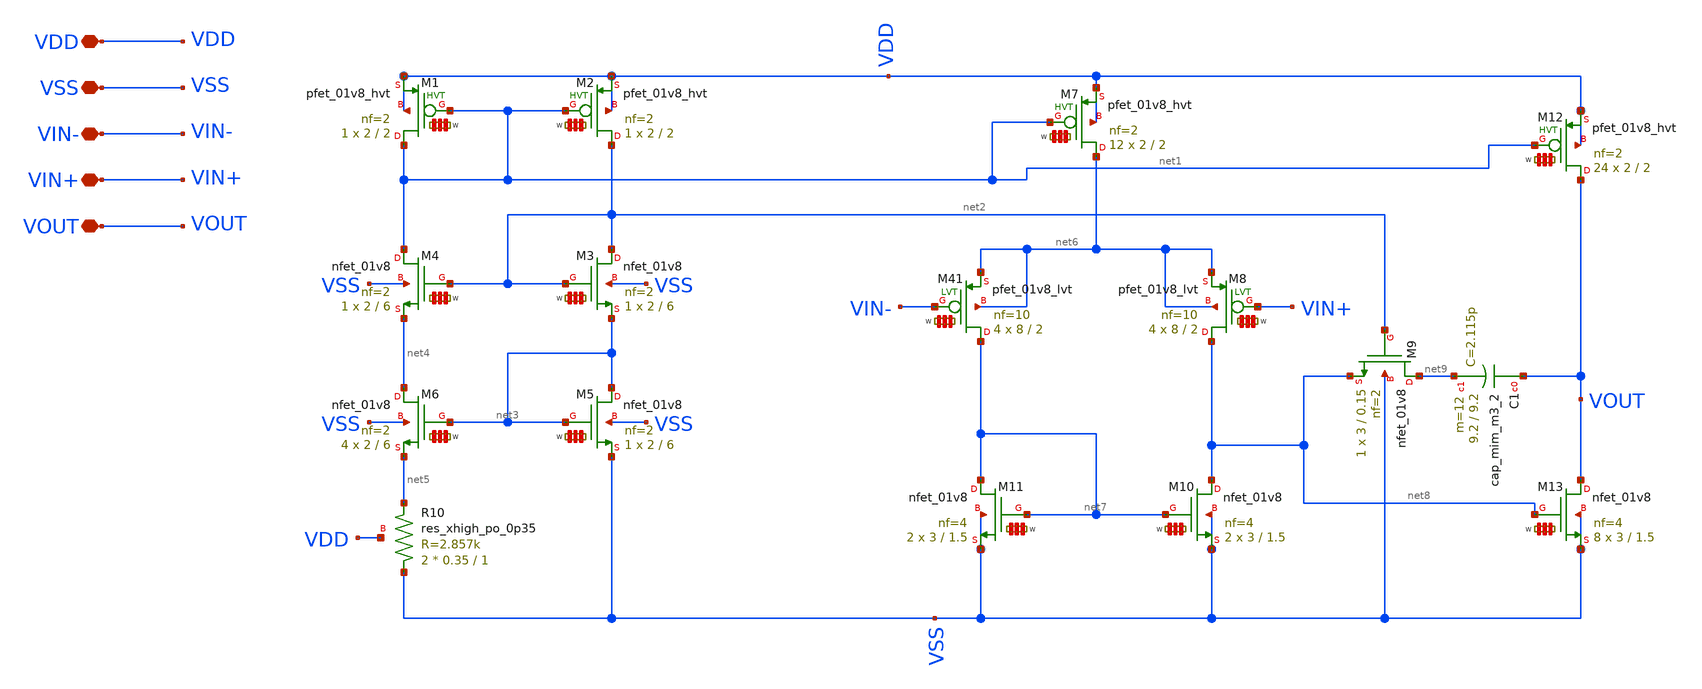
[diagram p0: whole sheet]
** sch_path: my_ip/sky130A/PMOS_2_stage_1_8_opamp_V1/op_amp.sch
**.subckt op_amp VDD VSS VIN- VIN+ VOUT
*.iopin VDD
*.iopin VSS
*.iopin VIN-
*.iopin VIN+
*.iopin VOUT
XM5 net3 net3 VSS VSS sky130_fd_pr__nfet_01v8 L=6 W='2 * 2 ' nf=2 ad='int((2 + 1)/2) * 2 / 2 * 0.29'
+ as='int((2 + 2)/2) * 2 / 2 * 0.29' pd='2*int((2 + 1)/2) * (2 / 2 + 0.29)' ps='2*int((2 + 2)/2) * (2 / 2 + 0.29)'
+ nrd='0.29 / 2 ' nrs='0.29 / 2 ' sa=0 sb=0 sd=0 mult=1 m=1
XM6 net4 net3 net5 VSS sky130_fd_pr__nfet_01v8 L=6 W='2 * 2 ' nf=2 ad='int((2 + 1)/2) * 2 / 2 * 0.29'
+ as='int((2 + 2)/2) * 2 / 2 * 0.29' pd='2*int((2 + 1)/2) * (2 / 2 + 0.29)' ps='2*int((2 + 2)/2) * (2 / 2 + 0.29)'
+ nrd='0.29 / 2 ' nrs='0.29 / 2 ' sa=0 sb=0 sd=0 mult=4 m=4
XM7 net6 net1 VDD VDD sky130_fd_pr__pfet_01v8_hvt L=2 W='2 * 2 ' nf=2 ad='int((2 + 1)/2) * 2 / 2 * 0.29'
+ as='int((2 + 2)/2) * 2 / 2 * 0.29' pd='2*int((2 + 1)/2) * (2 / 2 + 0.29)' ps='2*int((2 + 2)/2) * (2 / 2 + 0.29)'
+ nrd='0.29 / 2 ' nrs='0.29 / 2 ' sa=0 sb=0 sd=0 mult=12 m=12
XM2 net2 net1 VDD VDD sky130_fd_pr__pfet_01v8_hvt L=2 W='2 * 2 ' nf=2 ad='int((2 + 1)/2) * 2 / 2 * 0.29'
+ as='int((2 + 2)/2) * 2 / 2 * 0.29' pd='2*int((2 + 1)/2) * (2 / 2 + 0.29)' ps='2*int((2 + 2)/2) * (2 / 2 + 0.29)'
+ nrd='0.29 / 2 ' nrs='0.29 / 2 ' sa=0 sb=0 sd=0 mult=1 m=1
XM1 net1 net1 VDD VDD sky130_fd_pr__pfet_01v8_hvt L=2 W='2 * 2 ' nf=2 ad='int((2 + 1)/2) * 2 / 2 * 0.29'
+ as='int((2 + 2)/2) * 2 / 2 * 0.29' pd='2*int((2 + 1)/2) * (2 / 2 + 0.29)' ps='2*int((2 + 2)/2) * (2 / 2 + 0.29)'
+ nrd='0.29 / 2 ' nrs='0.29 / 2 ' sa=0 sb=0 sd=0 mult=1 m=1
XR10 VSS net5 VDD sky130_fd_pr__res_xhigh_po_0p35 L=1 mult=2 m=2
XM4 net1 net2 net4 VSS sky130_fd_pr__nfet_01v8 L=6 W='2 * 2 ' nf=2 ad='int((2 + 1)/2) * 2 / 2 * 0.29'
+ as='int((2 + 2)/2) * 2 / 2 * 0.29' pd='2*int((2 + 1)/2) * (2 / 2 + 0.29)' ps='2*int((2 + 2)/2) * (2 / 2 + 0.29)'
+ nrd='0.29 / 2 ' nrs='0.29 / 2 ' sa=0 sb=0 sd=0 mult=1 m=1
XM3 net2 net2 net3 VSS sky130_fd_pr__nfet_01v8 L=6 W='2 * 2 ' nf=2 ad='int((2 + 1)/2) * 2 / 2 * 0.29'
+ as='int((2 + 2)/2) * 2 / 2 * 0.29' pd='2*int((2 + 1)/2) * (2 / 2 + 0.29)' ps='2*int((2 + 2)/2) * (2 / 2 + 0.29)'
+ nrd='0.29 / 2 ' nrs='0.29 / 2 ' sa=0 sb=0 sd=0 mult=1 m=1
XM10 net8 net7 VSS VSS sky130_fd_pr__nfet_01v8 L=1.5 W='3 * 4 ' nf=4 ad='int((4 + 1)/2) * 3 / 4 * 0.29'
+ as='int((4 + 2)/2) * 3 / 4 * 0.29' pd='2*int((4 + 1)/2) * (3 / 4 + 0.29)' ps='2*int((4 + 2)/2) * (3 / 4 + 0.29)'
+ nrd='0.29 / 3 ' nrs='0.29 / 3 ' sa=0 sb=0 sd=0 mult=2 m=2
XM11 net7 net7 VSS VSS sky130_fd_pr__nfet_01v8 L=1.5 W='3 * 4 ' nf=4 ad='int((4 + 1)/2) * 3 / 4 * 0.29'
+ as='int((4 + 2)/2) * 3 / 4 * 0.29' pd='2*int((4 + 1)/2) * (3 / 4 + 0.29)' ps='2*int((4 + 2)/2) * (3 / 4 + 0.29)'
+ nrd='0.29 / 3 ' nrs='0.29 / 3 ' sa=0 sb=0 sd=0 mult=2 m=2
XM12 VOUT net1 VDD VDD sky130_fd_pr__pfet_01v8_hvt L=2 W='2 * 2 ' nf=2 ad='int((2 + 1)/2) * 2 / 2 * 0.29'
+ as='int((2 + 2)/2) * 2 / 2 * 0.29' pd='2*int((2 + 1)/2) * (2 / 2 + 0.29)' ps='2*int((2 + 2)/2) * (2 / 2 + 0.29)'
+ nrd='0.29 / 2 ' nrs='0.29 / 2 ' sa=0 sb=0 sd=0 mult=24 m=24
XM13 VOUT net8 VSS VSS sky130_fd_pr__nfet_01v8 L=1.5 W='3 * 4 ' nf=4 ad='int((4 + 1)/2) * 3 / 4 * 0.29'
+ as='int((4 + 2)/2) * 3 / 4 * 0.29' pd='2*int((4 + 1)/2) * (3 / 4 + 0.29)' ps='2*int((4 + 2)/2) * (3 / 4 + 0.29)'
+ nrd='0.29 / 3 ' nrs='0.29 / 3 ' sa=0 sb=0 sd=0 mult=8 m=8
XC1 VOUT net9 sky130_fd_pr__cap_mim_m3_2 W=9.2 L=9.2 MF=12 m=12
XM41 net7 VIN- net6 net6 sky130_fd_pr__pfet_01v8_lvt L=2 W='8 * 10 ' nf=10 ad='int((10 + 1)/2) * 8 / 10 * 0.29'
+ as='int((10 + 2)/2) * 8 / 10 * 0.29' pd='2*int((10 + 1)/2) * (8 / 10 + 0.29)' ps='2*int((10 + 2)/2) * (8 / 10 + 0.29)'
+ nrd='0.29 / 8 ' nrs='0.29 / 8 ' sa=0 sb=0 sd=0 mult=4 m=4
XM8 net8 VIN+ net6 net6 sky130_fd_pr__pfet_01v8_lvt L=2 W='8 * 10 ' nf=10 ad='int((10 + 1)/2) * 8 / 10 * 0.29'
+ as='int((10 + 2)/2) * 8 / 10 * 0.29' pd='2*int((10 + 1)/2) * (8 / 10 + 0.29)' ps='2*int((10 + 2)/2) * (8 / 10 + 0.29)'
+ nrd='0.29 / 8 ' nrs='0.29 / 8 ' sa=0 sb=0 sd=0 mult=4 m=4
XM9 net9 net2 net8 VSS sky130_fd_pr__nfet_01v8 L=0.15 W=3 nf=2 ad='int((2 + 1)/2) * 3 / 2 * 0.29' as='int((2 + 2)/2) * 3 / 2 * 0.29'
+ pd='2*int((2 + 1)/2) * (3 / 2 + 0.29)' ps='2*int((2 + 2)/2) * (3 / 2 + 0.29)' nrd='0.29 / 3 ' nrs='0.29 / 3 '
+ sa=0 sb=0 sd=0 mult=1 m=1
**.ends
.end
